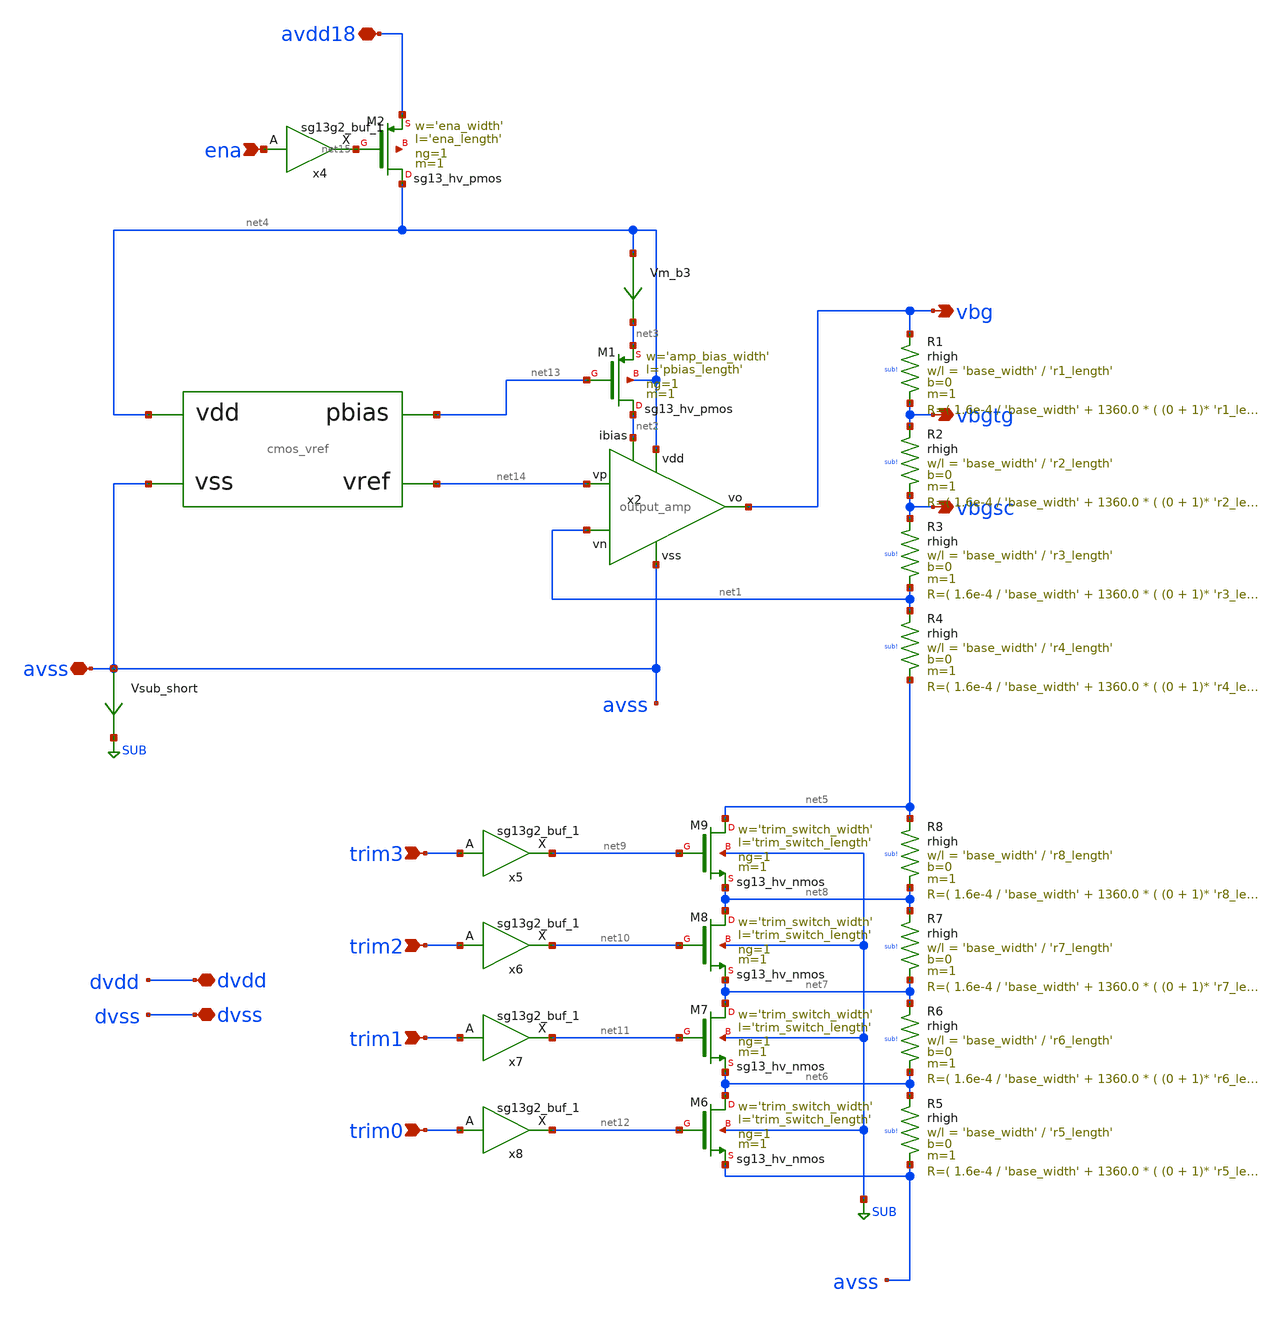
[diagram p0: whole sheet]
** sch_path: sch/top/top_default.sch
**.subckt top_default vbg avss dvdd dvss vbgsc vbgtg trim3 trim2 trim1 trim0 avdd18 ena
*.opin vbg
*.iopin avss
*.iopin dvdd
*.iopin dvss
*.opin vbgsc
*.opin vbgtg
*.ipin trim3
*.ipin trim2
*.ipin trim1
*.ipin trim0
*.iopin avdd18
*.ipin ena
x2 net4 vbg net14 net1 net2 avss output_amp
Vm_b3 net4 net3 0
.save i(vm_b3)
Vsub_short avss SUB 0
.save i(vsub_short)
XM1 net2 net13 net3 net4 sg13_hv_pmos w='amp_bias_width' l='pbias_length' ng=1 m=1 mm_ok=1
x5 net9 trim3 VDD VSS sg13g2_buf_1
x6 net10 trim2 VDD VSS sg13g2_buf_1
x7 net11 trim1 VDD VSS sg13g2_buf_1
x8 net12 trim0 VDD VSS sg13g2_buf_1
XR1 vbg vbgtg sub! rhigh w='base_width' l='r1_length' m=1 b=0 mm_ok=1
XR2 vbgtg vbgsc sub! rhigh w='base_width' l='r2_length' m=1 b=0 mm_ok=1
XR3 vbgsc net1 sub! rhigh w='base_width' l='r3_length' m=1 b=0 mm_ok=1
XR4 net1 net5 sub! rhigh w='base_width' l='r4_length' m=1 b=0 mm_ok=1
XM6 net6 net12 avss SUB sg13_hv_nmos w='trim_switch_width' l='trim_switch_length' ng=1 m=1 mm_ok=1
XM7 net7 net11 net6 SUB sg13_hv_nmos w='trim_switch_width' l='trim_switch_length' ng=1 m=1 mm_ok=1
XM8 net8 net10 net7 SUB sg13_hv_nmos w='trim_switch_width' l='trim_switch_length' ng=1 m=1 mm_ok=1
XM9 net5 net9 net8 SUB sg13_hv_nmos w='trim_switch_width' l='trim_switch_length' ng=1 m=1 mm_ok=1
XR5 net6 avss sub! rhigh w='base_width' l='r5_length' m=1 b=0 mm_ok=1
XR6 net7 net6 sub! rhigh w='base_width' l='r6_length' m=1 b=0 mm_ok=1
XR7 net8 net7 sub! rhigh w='base_width' l='r7_length' m=1 b=0 mm_ok=1
XR8 net5 net8 sub! rhigh w='base_width' l='r8_length' m=1 b=0 mm_ok=1
X1 net14 net4 avss net13 cmos_vref
x4 net15 ena VDD VSS sg13g2_buf_1
XM2 net4 net15 avdd18 net16 sg13_hv_pmos w='ena_width' l='ena_length' ng=1 m=1 mm_ok=1
**.ends
.GLOBAL SUB
.end
